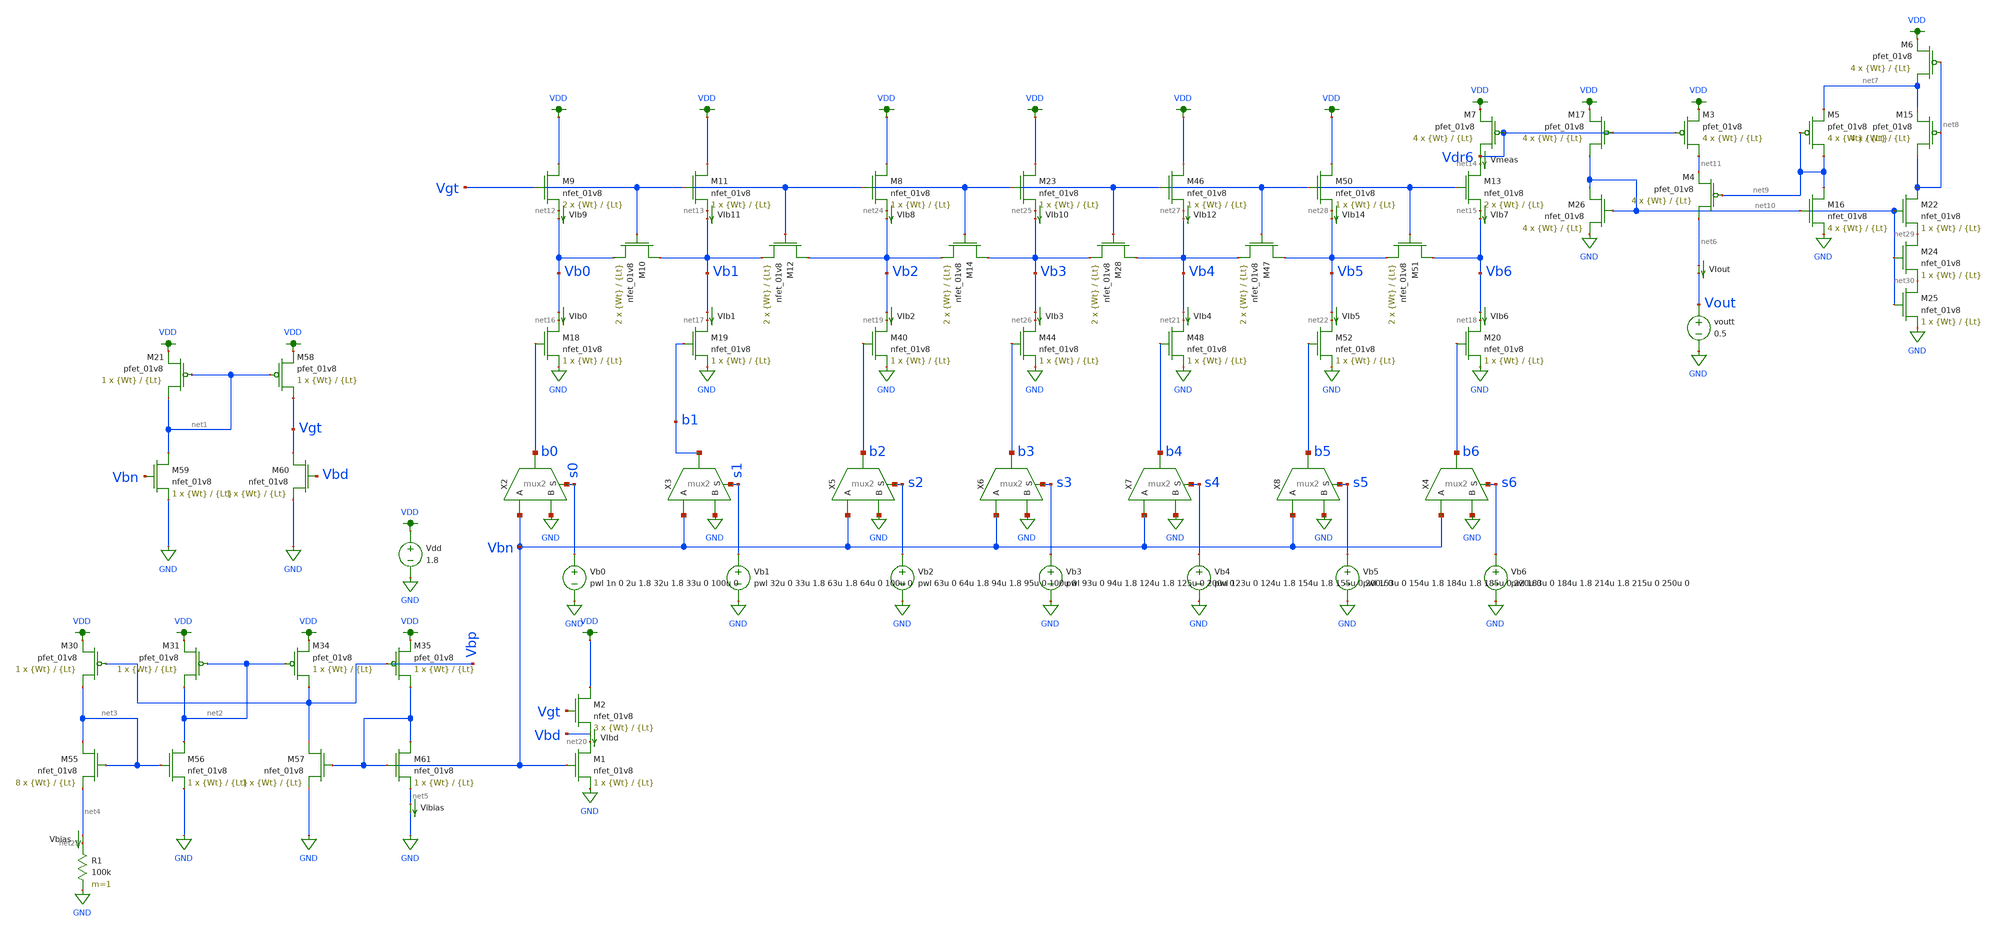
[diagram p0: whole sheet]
** sch_path: schematic/archive/dac7_test_josh_cascode_idnl.sch
**.subckt dac7_test_josh_cascode_idnl
X2 b0 Vbn GND s0 mux2
X3 b1 Vbn GND s1 mux2
Vdd VDD GND 1.8
Vb0 s0 GND pwl 1n 0 2u 1.8 32u 1.8 33u 0 100u 0
Vb1 s1 GND pwl 32u 0 33u 1.8 63u 1.8 64u 0 100u 0
Vb2 s2 GND pwl 63u 0 64u 1.8 94u 1.8 95u 0 100u 0
XM9 VDD Vgt net12 GND sky130_fd_pr__nfet_01v8 L={Lt} W={Wt} nf=1 ad='int((nf+1)/2) * W/nf * 0.29' as='int((nf+2)/2) * W/nf * 0.29'
+ pd='2*int((nf+1)/2) * (W/nf + 0.29)' ps='2*int((nf+2)/2) * (W/nf + 0.29)' nrd='0.29 / W' nrs='0.29 / W'
+ sa=0 sb=0 sd=0 mult=2 m=2
XM10 Vb1 Vgt Vb0 GND sky130_fd_pr__nfet_01v8 L={Lt} W={Wt} nf=1 ad='int((nf+1)/2) * W/nf * 0.29' as='int((nf+2)/2) * W/nf * 0.29'
+ pd='2*int((nf+1)/2) * (W/nf + 0.29)' ps='2*int((nf+2)/2) * (W/nf + 0.29)' nrd='0.29 / W' nrs='0.29 / W'
+ sa=0 sb=0 sd=0 mult=2 m=2
XM11 VDD Vgt net13 GND sky130_fd_pr__nfet_01v8 L={Lt} W={Wt} nf=1 ad='int((nf+1)/2) * W/nf * 0.29' as='int((nf+2)/2) * W/nf * 0.29'
+ pd='2*int((nf+1)/2) * (W/nf + 0.29)' ps='2*int((nf+2)/2) * (W/nf + 0.29)' nrd='0.29 / W' nrs='0.29 / W'
+ sa=0 sb=0 sd=0 mult=1 m=1
XM12 Vb2 Vgt Vb1 GND sky130_fd_pr__nfet_01v8 L={Lt} W={Wt} nf=1 ad='int((nf+1)/2) * W/nf * 0.29' as='int((nf+2)/2) * W/nf * 0.29'
+ pd='2*int((nf+1)/2) * (W/nf + 0.29)' ps='2*int((nf+2)/2) * (W/nf + 0.29)' nrd='0.29 / W' nrs='0.29 / W'
+ sa=0 sb=0 sd=0 mult=2 m=2
XM13 net14 Vgt net15 GND sky130_fd_pr__nfet_01v8 L={Lt} W={Wt} nf=1 ad='int((nf+1)/2) * W/nf * 0.29'
+ as='int((nf+2)/2) * W/nf * 0.29' pd='2*int((nf+1)/2) * (W/nf + 0.29)' ps='2*int((nf+2)/2) * (W/nf + 0.29)'
+ nrd='0.29 / W' nrs='0.29 / W' sa=0 sb=0 sd=0 mult=2 m=2
XM18 net16 b0 GND GND sky130_fd_pr__nfet_01v8 L={Lt} W={Wt} nf=1 ad='int((nf+1)/2) * W/nf * 0.29' as='int((nf+2)/2) * W/nf * 0.29'
+ pd='2*int((nf+1)/2) * (W/nf + 0.29)' ps='2*int((nf+2)/2) * (W/nf + 0.29)' nrd='0.29 / W' nrs='0.29 / W'
+ sa=0 sb=0 sd=0 mult=1 m=1
XM19 net17 b1 GND GND sky130_fd_pr__nfet_01v8 L={Lt} W={Wt} nf=1 ad='int((nf+1)/2) * W/nf * 0.29' as='int((nf+2)/2) * W/nf * 0.29'
+ pd='2*int((nf+1)/2) * (W/nf + 0.29)' ps='2*int((nf+2)/2) * (W/nf + 0.29)' nrd='0.29 / W' nrs='0.29 / W'
+ sa=0 sb=0 sd=0 mult=1 m=1
XM20 net18 b6 GND GND sky130_fd_pr__nfet_01v8 L={Lt} W={Wt} nf=1 ad='int((nf+1)/2) * W/nf * 0.29' as='int((nf+2)/2) * W/nf * 0.29'
+ pd='2*int((nf+1)/2) * (W/nf + 0.29)' ps='2*int((nf+2)/2) * (W/nf + 0.29)' nrd='0.29 / W' nrs='0.29 / W'
+ sa=0 sb=0 sd=0 mult=1 m=1
Vmeas Vdr6 net14 0
.save i(vmeas)
VIb0 Vb0 net16 0
.save i(vib0)
VIb1 Vb1 net17 0
.save i(vib1)
VIb2 Vb2 net19 0
.save i(vib2)
XM1 net20 Vbn GND GND sky130_fd_pr__nfet_01v8 L={Lt} W={Wt} nf=1 ad='int((nf+1)/2) * W/nf * 0.29' as='int((nf+2)/2) * W/nf * 0.29'
+ pd='2*int((nf+1)/2) * (W/nf + 0.29)' ps='2*int((nf+2)/2) * (W/nf + 0.29)' nrd='0.29 / W' nrs='0.29 / W'
+ sa=0 sb=0 sd=0 mult=1 m=1
VIbd Vbd net20 0
.save i(vibd)
VIb4 Vb4 net21 0
.save i(vib4)
VIb5 Vb5 net22 0
.save i(vib5)
VIb6 Vb6 net18 0
.save i(vib6)
VIout net6 Vout 0
.save i(viout)
XM2 VDD Vgt Vbd GND sky130_fd_pr__nfet_01v8 L={Lt} W={Wt} nf=1 ad='int((nf+1)/2) * W/nf * 0.29' as='int((nf+2)/2) * W/nf * 0.29'
+ pd='2*int((nf+1)/2) * (W/nf + 0.29)' ps='2*int((nf+2)/2) * (W/nf + 0.29)' nrd='0.29 / W' nrs='0.29 / W'
+ sa=0 sb=0 sd=0 mult=3 m=3
XM21 net1 net1 VDD VDD sky130_fd_pr__pfet_01v8 L={Lt} W={Wt} nf=1 ad='int((nf+1)/2) * W/nf * 0.29' as='int((nf+2)/2) * W/nf * 0.29'
+ pd='2*int((nf+1)/2) * (W/nf + 0.29)' ps='2*int((nf+2)/2) * (W/nf + 0.29)' nrd='0.29 / W' nrs='0.29 / W'
+ sa=0 sb=0 sd=0 mult=1 m=1
XM58 Vgt net1 VDD VDD sky130_fd_pr__pfet_01v8 L={Lt} W={Wt} nf=1 ad='int((nf+1)/2) * W/nf * 0.29' as='int((nf+2)/2) * W/nf * 0.29'
+ pd='2*int((nf+1)/2) * (W/nf + 0.29)' ps='2*int((nf+2)/2) * (W/nf + 0.29)' nrd='0.29 / W' nrs='0.29 / W'
+ sa=0 sb=0 sd=0 mult=1 m=1
XM59 net1 Vbn GND GND sky130_fd_pr__nfet_01v8 L={Lt} W={Wt} nf=1 ad='int((nf+1)/2) * W/nf * 0.29' as='int((nf+2)/2) * W/nf * 0.29'
+ pd='2*int((nf+1)/2) * (W/nf + 0.29)' ps='2*int((nf+2)/2) * (W/nf + 0.29)' nrd='0.29 / W' nrs='0.29 / W'
+ sa=0 sb=0 sd=0 mult=1 m=1
XM60 Vgt Vbd GND GND sky130_fd_pr__nfet_01v8 L={Lt} W={Wt} nf=1 ad='int((nf+1)/2) * W/nf * 0.29' as='int((nf+2)/2) * W/nf * 0.29'
+ pd='2*int((nf+1)/2) * (W/nf + 0.29)' ps='2*int((nf+2)/2) * (W/nf + 0.29)' nrd='0.29 / W' nrs='0.29 / W'
+ sa=0 sb=0 sd=0 mult=1 m=1
R1 net23 GND 100k m=1
Vbias net4 net23 0
.save i(vbias)
X5 b2 Vbn GND s2 mux2
Vb3 s3 GND pwl 93u 0 94u 1.8 124u 1.8 125u 0 200u 0
XM8 VDD Vgt net24 GND sky130_fd_pr__nfet_01v8 L={Lt} W={Wt} nf=1 ad='int((nf+1)/2) * W/nf * 0.29' as='int((nf+2)/2) * W/nf * 0.29'
+ pd='2*int((nf+1)/2) * (W/nf + 0.29)' ps='2*int((nf+2)/2) * (W/nf + 0.29)' nrd='0.29 / W' nrs='0.29 / W'
+ sa=0 sb=0 sd=0 mult=1 m=1
XM14 Vb3 Vgt Vb2 GND sky130_fd_pr__nfet_01v8 L={Lt} W={Wt} nf=1 ad='int((nf+1)/2) * W/nf * 0.29' as='int((nf+2)/2) * W/nf * 0.29'
+ pd='2*int((nf+1)/2) * (W/nf + 0.29)' ps='2*int((nf+2)/2) * (W/nf + 0.29)' nrd='0.29 / W' nrs='0.29 / W'
+ sa=0 sb=0 sd=0 mult=2 m=2
XM40 net19 b2 GND GND sky130_fd_pr__nfet_01v8 L={Lt} W={Wt} nf=1 ad='int((nf+1)/2) * W/nf * 0.29' as='int((nf+2)/2) * W/nf * 0.29'
+ pd='2*int((nf+1)/2) * (W/nf + 0.29)' ps='2*int((nf+2)/2) * (W/nf + 0.29)' nrd='0.29 / W' nrs='0.29 / W'
+ sa=0 sb=0 sd=0 mult=1 m=1
VIb7 net15 Vb6 0
.save i(vib7)
VIb8 net24 Vb2 0
.save i(vib8)
X6 b3 Vbn GND s3 mux2
Vb4 s4 GND pwl 123u 0 124u 1.8 154u 1.8 155u 0 200u 0
XM23 VDD Vgt net25 GND sky130_fd_pr__nfet_01v8 L={Lt} W={Wt} nf=1 ad='int((nf+1)/2) * W/nf * 0.29' as='int((nf+2)/2) * W/nf * 0.29'
+ pd='2*int((nf+1)/2) * (W/nf + 0.29)' ps='2*int((nf+2)/2) * (W/nf + 0.29)' nrd='0.29 / W' nrs='0.29 / W'
+ sa=0 sb=0 sd=0 mult=1 m=1
XM28 Vb4 Vgt Vb3 GND sky130_fd_pr__nfet_01v8 L={Lt} W={Wt} nf=1 ad='int((nf+1)/2) * W/nf * 0.29' as='int((nf+2)/2) * W/nf * 0.29'
+ pd='2*int((nf+1)/2) * (W/nf + 0.29)' ps='2*int((nf+2)/2) * (W/nf + 0.29)' nrd='0.29 / W' nrs='0.29 / W'
+ sa=0 sb=0 sd=0 mult=2 m=2
XM44 net26 b3 GND GND sky130_fd_pr__nfet_01v8 L={Lt} W={Wt} nf=1 ad='int((nf+1)/2) * W/nf * 0.29' as='int((nf+2)/2) * W/nf * 0.29'
+ pd='2*int((nf+1)/2) * (W/nf + 0.29)' ps='2*int((nf+2)/2) * (W/nf + 0.29)' nrd='0.29 / W' nrs='0.29 / W'
+ sa=0 sb=0 sd=0 mult=1 m=1
VIb3 Vb3 net26 0
.save i(vib3)
VIb10 net25 Vb3 0
.save i(vib10)
X7 b4 Vbn GND s4 mux2
Vb5 s5 GND pwl 153u 0 154u 1.8 184u 1.8 185u 0 220u 0
XM46 VDD Vgt net27 GND sky130_fd_pr__nfet_01v8 L={Lt} W={Wt} nf=1 ad='int((nf+1)/2) * W/nf * 0.29' as='int((nf+2)/2) * W/nf * 0.29'
+ pd='2*int((nf+1)/2) * (W/nf + 0.29)' ps='2*int((nf+2)/2) * (W/nf + 0.29)' nrd='0.29 / W' nrs='0.29 / W'
+ sa=0 sb=0 sd=0 mult=1 m=1
XM47 Vb5 Vgt Vb4 GND sky130_fd_pr__nfet_01v8 L={Lt} W={Wt} nf=1 ad='int((nf+1)/2) * W/nf * 0.29' as='int((nf+2)/2) * W/nf * 0.29'
+ pd='2*int((nf+1)/2) * (W/nf + 0.29)' ps='2*int((nf+2)/2) * (W/nf + 0.29)' nrd='0.29 / W' nrs='0.29 / W'
+ sa=0 sb=0 sd=0 mult=2 m=2
XM48 net21 b4 GND GND sky130_fd_pr__nfet_01v8 L={Lt} W={Wt} nf=1 ad='int((nf+1)/2) * W/nf * 0.29' as='int((nf+2)/2) * W/nf * 0.29'
+ pd='2*int((nf+1)/2) * (W/nf + 0.29)' ps='2*int((nf+2)/2) * (W/nf + 0.29)' nrd='0.29 / W' nrs='0.29 / W'
+ sa=0 sb=0 sd=0 mult=1 m=1
VIb9 net12 Vb0 0
.save i(vib9)
VIb12 net27 Vb4 0
.save i(vib12)
X8 b5 Vbn GND s5 mux2
XM50 VDD Vgt net28 GND sky130_fd_pr__nfet_01v8 L={Lt} W={Wt} nf=1 ad='int((nf+1)/2) * W/nf * 0.29' as='int((nf+2)/2) * W/nf * 0.29'
+ pd='2*int((nf+1)/2) * (W/nf + 0.29)' ps='2*int((nf+2)/2) * (W/nf + 0.29)' nrd='0.29 / W' nrs='0.29 / W'
+ sa=0 sb=0 sd=0 mult=1 m=1
XM51 Vb6 Vgt Vb5 GND sky130_fd_pr__nfet_01v8 L={Lt} W={Wt} nf=1 ad='int((nf+1)/2) * W/nf * 0.29' as='int((nf+2)/2) * W/nf * 0.29'
+ pd='2*int((nf+1)/2) * (W/nf + 0.29)' ps='2*int((nf+2)/2) * (W/nf + 0.29)' nrd='0.29 / W' nrs='0.29 / W'
+ sa=0 sb=0 sd=0 mult=2 m=2
XM52 net22 b5 GND GND sky130_fd_pr__nfet_01v8 L={Lt} W={Wt} nf=1 ad='int((nf+1)/2) * W/nf * 0.29' as='int((nf+2)/2) * W/nf * 0.29'
+ pd='2*int((nf+1)/2) * (W/nf + 0.29)' ps='2*int((nf+2)/2) * (W/nf + 0.29)' nrd='0.29 / W' nrs='0.29 / W'
+ sa=0 sb=0 sd=0 mult=1 m=1
VIb11 net13 Vb1 0
.save i(vib11)
VIb14 net28 Vb5 0
.save i(vib14)
Vb6 s6 GND pwl 183u 0 184u 1.8 214u 1.8 215u 0 250u 0
X4 b6 Vbn GND s6 mux2
XM30 net3 Vbp VDD VDD sky130_fd_pr__pfet_01v8 L={Lt} W={Wt} nf=1 ad='int((nf+1)/2) * W/nf * 0.29' as='int((nf+2)/2) * W/nf * 0.29'
+ pd='2*int((nf+1)/2) * (W/nf + 0.29)' ps='2*int((nf+2)/2) * (W/nf + 0.29)' nrd='0.29 / W' nrs='0.29 / W'
+ sa=0 sb=0 sd=0 mult=1 m=1
XM31 net2 net2 VDD VDD sky130_fd_pr__pfet_01v8 L={Lt} W={Wt} nf=1 ad='int((nf+1)/2) * W/nf * 0.29' as='int((nf+2)/2) * W/nf * 0.29'
+ pd='2*int((nf+1)/2) * (W/nf + 0.29)' ps='2*int((nf+2)/2) * (W/nf + 0.29)' nrd='0.29 / W' nrs='0.29 / W'
+ sa=0 sb=0 sd=0 mult=1 m=1
XM34 Vbp net2 VDD VDD sky130_fd_pr__pfet_01v8 L={Lt} W={Wt} nf=1 ad='int((nf+1)/2) * W/nf * 0.29' as='int((nf+2)/2) * W/nf * 0.29'
+ pd='2*int((nf+1)/2) * (W/nf + 0.29)' ps='2*int((nf+2)/2) * (W/nf + 0.29)' nrd='0.29 / W' nrs='0.29 / W'
+ sa=0 sb=0 sd=0 mult=1 m=1
XM35 Vbn Vbp VDD VDD sky130_fd_pr__pfet_01v8 L={Lt} W={Wt} nf=1 ad='int((nf+1)/2) * W/nf * 0.29' as='int((nf+2)/2) * W/nf * 0.29'
+ pd='2*int((nf+1)/2) * (W/nf + 0.29)' ps='2*int((nf+2)/2) * (W/nf + 0.29)' nrd='0.29 / W' nrs='0.29 / W'
+ sa=0 sb=0 sd=0 mult=1 m=1
XM55 net3 net3 net4 GND sky130_fd_pr__nfet_01v8 L={Lt} W={Wt} nf=1 ad='int((nf+1)/2) * W/nf * 0.29' as='int((nf+2)/2) * W/nf * 0.29'
+ pd='2*int((nf+1)/2) * (W/nf + 0.29)' ps='2*int((nf+2)/2) * (W/nf + 0.29)' nrd='0.29 / W' nrs='0.29 / W'
+ sa=0 sb=0 sd=0 mult=8 m=8
XM56 net2 net3 GND GND sky130_fd_pr__nfet_01v8 L={Lt} W={Wt} nf=1 ad='int((nf+1)/2) * W/nf * 0.29' as='int((nf+2)/2) * W/nf * 0.29'
+ pd='2*int((nf+1)/2) * (W/nf + 0.29)' ps='2*int((nf+2)/2) * (W/nf + 0.29)' nrd='0.29 / W' nrs='0.29 / W'
+ sa=0 sb=0 sd=0 mult=1 m=1
XM57 Vbp Vbn GND GND sky130_fd_pr__nfet_01v8 L={Lt} W={Wt} nf=1 ad='int((nf+1)/2) * W/nf * 0.29' as='int((nf+2)/2) * W/nf * 0.29'
+ pd='2*int((nf+1)/2) * (W/nf + 0.29)' ps='2*int((nf+2)/2) * (W/nf + 0.29)' nrd='0.29 / W' nrs='0.29 / W'
+ sa=0 sb=0 sd=0 mult=1 m=1
XM61 Vbn Vbn net5 GND sky130_fd_pr__nfet_01v8 L={Lt} W={Wt} nf=1 ad='int((nf+1)/2) * W/nf * 0.29' as='int((nf+2)/2) * W/nf * 0.29'
+ pd='2*int((nf+1)/2) * (W/nf + 0.29)' ps='2*int((nf+2)/2) * (W/nf + 0.29)' nrd='0.29 / W' nrs='0.29 / W'
+ sa=0 sb=0 sd=0 mult=1 m=1
Vibias net5 GND 0
.save i(vibias)
voutt Vout GND 0.5
XM7 Vdr6 Vdr6 VDD VDD sky130_fd_pr__pfet_01v8 L={Lt} W={Wt} nf=1 ad='int((nf+1)/2) * W/nf * 0.29' as='int((nf+2)/2) * W/nf * 0.29'
+ pd='2*int((nf+1)/2) * (W/nf + 0.29)' ps='2*int((nf+2)/2) * (W/nf + 0.29)' nrd='0.29 / W' nrs='0.29 / W'
+ sa=0 sb=0 sd=0 mult=4 m=4
XM3 net11 Vdr6 VDD VDD sky130_fd_pr__pfet_01v8 L={Lt} W={Wt} nf=1 ad='int((nf+1)/2) * W/nf * 0.29' as='int((nf+2)/2) * W/nf * 0.29'
+ pd='2*int((nf+1)/2) * (W/nf + 0.29)' ps='2*int((nf+2)/2) * (W/nf + 0.29)' nrd='0.29 / W' nrs='0.29 / W'
+ sa=0 sb=0 sd=0 mult=4 m=4
XM4 net6 net9 net11 VDD sky130_fd_pr__pfet_01v8 L={Lt} W={Wt} nf=1 ad='int((nf+1)/2) * W/nf * 0.29' as='int((nf+2)/2) * W/nf * 0.29'
+ pd='2*int((nf+1)/2) * (W/nf + 0.29)' ps='2*int((nf+2)/2) * (W/nf + 0.29)' nrd='0.29 / W' nrs='0.29 / W'
+ sa=0 sb=0 sd=0 mult=4 m=4
XM5 net9 net9 net7 VDD sky130_fd_pr__pfet_01v8 L={Lt} W={Wt} nf=1 ad='int((nf+1)/2) * W/nf * 0.29' as='int((nf+2)/2) * W/nf * 0.29'
+ pd='2*int((nf+1)/2) * (W/nf + 0.29)' ps='2*int((nf+2)/2) * (W/nf + 0.29)' nrd='0.29 / W' nrs='0.29 / W'
+ sa=0 sb=0 sd=0 mult=4 m=4
XM6 net7 net8 VDD VDD sky130_fd_pr__pfet_01v8 L={Lt} W={Wt} nf=1 ad='int((nf+1)/2) * W/nf * 0.29' as='int((nf+2)/2) * W/nf * 0.29'
+ pd='2*int((nf+1)/2) * (W/nf + 0.29)' ps='2*int((nf+2)/2) * (W/nf + 0.29)' nrd='0.29 / W' nrs='0.29 / W'
+ sa=0 sb=0 sd=0 mult=4 m=4
XM15 net8 net8 net7 VDD sky130_fd_pr__pfet_01v8 L={Lt} W={Wt} nf=1 ad='int((nf+1)/2) * W/nf * 0.29' as='int((nf+2)/2) * W/nf * 0.29'
+ pd='2*int((nf+1)/2) * (W/nf + 0.29)' ps='2*int((nf+2)/2) * (W/nf + 0.29)' nrd='0.29 / W' nrs='0.29 / W'
+ sa=0 sb=0 sd=0 mult=4 m=4
XM16 net9 net10 GND GND sky130_fd_pr__nfet_01v8 L={Lt} W={Wt} nf=1 ad='int((nf+1)/2) * W/nf * 0.29' as='int((nf+2)/2) * W/nf * 0.29'
+ pd='2*int((nf+1)/2) * (W/nf + 0.29)' ps='2*int((nf+2)/2) * (W/nf + 0.29)' nrd='0.29 / W' nrs='0.29 / W'
+ sa=0 sb=0 sd=0 mult=4 m=4
XM22 net8 net10 net29 GND sky130_fd_pr__nfet_01v8 L={Lt} W={Wt} nf=1 ad='int((nf+1)/2) * W/nf * 0.29'
+ as='int((nf+2)/2) * W/nf * 0.29' pd='2*int((nf+1)/2) * (W/nf + 0.29)' ps='2*int((nf+2)/2) * (W/nf + 0.29)'
+ nrd='0.29 / W' nrs='0.29 / W' sa=0 sb=0 sd=0 mult=1 m=1
XM24 net29 net10 net30 GND sky130_fd_pr__nfet_01v8 L={Lt} W={Wt} nf=1 ad='int((nf+1)/2) * W/nf * 0.29'
+ as='int((nf+2)/2) * W/nf * 0.29' pd='2*int((nf+1)/2) * (W/nf + 0.29)' ps='2*int((nf+2)/2) * (W/nf + 0.29)'
+ nrd='0.29 / W' nrs='0.29 / W' sa=0 sb=0 sd=0 mult=1 m=1
XM25 net30 net10 GND GND sky130_fd_pr__nfet_01v8 L={Lt} W={Wt} nf=1 ad='int((nf+1)/2) * W/nf * 0.29'
+ as='int((nf+2)/2) * W/nf * 0.29' pd='2*int((nf+1)/2) * (W/nf + 0.29)' ps='2*int((nf+2)/2) * (W/nf + 0.29)'
+ nrd='0.29 / W' nrs='0.29 / W' sa=0 sb=0 sd=0 mult=1 m=1
XM17 net10 Vdr6 VDD VDD sky130_fd_pr__pfet_01v8 L={Lt} W={Wt} nf=1 ad='int((nf+1)/2) * W/nf * 0.29' as='int((nf+2)/2) * W/nf * 0.29'
+ pd='2*int((nf+1)/2) * (W/nf + 0.29)' ps='2*int((nf+2)/2) * (W/nf + 0.29)' nrd='0.29 / W' nrs='0.29 / W'
+ sa=0 sb=0 sd=0 mult=4 m=4
XM26 net10 net10 GND GND sky130_fd_pr__nfet_01v8 L={Lt} W={Wt} nf=1 ad='int((nf+1)/2) * W/nf * 0.29'
+ as='int((nf+2)/2) * W/nf * 0.29' pd='2*int((nf+1)/2) * (W/nf + 0.29)' ps='2*int((nf+2)/2) * (W/nf + 0.29)'
+ nrd='0.29 / W' nrs='0.29 / W' sa=0 sb=0 sd=0 mult=4 m=4
**** begin user architecture code

.option wnflag=1
.param MC_SWITCH=1.0
.lib ~/skywater/skywater-pdk/libraries/sky130_fd_pr_ngspice/latest/models/sky130.lib.spice tt


.param Wt = 16
.param Lt = 4
.control
*** change W and L for the next two lines as well !***
  let myW = 16
  let myL = 4
  set wr_singlescale
  let runs = 10
  let run = 1
  while run <= runs
    set appendwrite = FALSE
    set wr_vecnames
    let code = 0
    while code < 64
      if code eq 0
        let b0 = 0
      else
        let b0 = (code % 2) * 1.8
      end
      if floor(code / 2) eq 0
        let b1 = 0
      else
        let b1 = (floor(code / 2) % 2) * 1.8
      end
      if floor(code / 4) eq 0
        let b2 = 0
      else
        let b2 = (floor(code / 4) % 2) * 1.8
      end
      if floor(code / 8) eq 0
        let b3 = 0
      else
        let b3 = floor(code / 8) % 2 * 1.8
      end
      if floor(code / 16) eq 0
        let b4 = 0
      else
        let b4 = floor(code / 16) % 2 * 1.8
      end
      if floor(code / 32) eq 0
        let b5 = 0
      else
        let b5 = floor(code / 32) % 2 * 1.8
      end
      if floor(code / 64) eq 0
        let b6 = 0
      else
        let b6 = floor(code / 64) % 2 * 1.8
      end
      alter vb0 $&b0
      alter vb1 $&b1
      alter vb2 $&b2
      alter vb3 $&b3
      alter vb4 $&b4
      alter vb5 $&b5
      alter vb6 $&b6
      save v(b0) v(b1) v(b2) v(b3) v(b4) v(b5) v(b6) i(vbias) i(viout) v(vout)
      op
      wrdata ~/Documents/MADVLSI-MP4/schematic/data/dac7cass_L{$&myL}W{$&myW}op-{$&run}.txt v(b0) v(b1)
+ v(b2) v(b3) v(b4) v(b5) v(b6) i(vbias) i(viout) v(vout)
      if code eq 0
        set appendwrite
        set wr_vecnames = FALSE
      end
      let code = code + 1
    end
    reset
    let run = run + 1
  end

  set appendwrite = FALSE
  reset
  set wr_singlescale
  set wr_vecnames
  alter vb0 1.8
  alter vb1 1.8
  alter vb2 1.8
  alter vb3 1.8
  alter vb4 1.8
  alter vb5 1.8
  alter vb6 1.8
  save v(b0) v(b1) v(b2) v(b3) v(b4) v(b5) v(b6) i(vbias) i(viout) v(vout)
  dc Voutt 0 1.8 0.01
  run
  wrdata ~/Documents/MADVLSI-MP4/schematic/data/dac7cass_L{$&myL}W{$&myW}vout-1.txt v(b0) v(b1) v(b2)
+ v(b3) v(b4) v(b5) v(b6) i(vbias) i(viout) v(vout)

  reset
  set wr_singlescale
  set wr_vecnames
  alter vb0 1.8
  alter vb1 1.8
  alter vb2 1.8
  alter vb3 1.8
  alter vb4 1.8
  alter vb5 1.8
  alter vb6 0
  save v(b0) v(b1) v(b2) v(b3) v(b4) v(b5) v(b6) i(vbias) i(viout) v(vout)
  dc Voutt 0 1.8 0.01
  run
  wrdata ~/Documents/MADVLSI-MP4/schematic/data/dac7cass_L{$&myL}W{$&myW}vout-2.txt v(b0) v(b1) v(b2)
+ v(b3) v(b4) v(b5) v(b6) i(vbias) i(viout) v(vout)

  reset
  set wr_singlescale
  set wr_vecnames
  alter vb0 1.8
  alter vb1 1.8
  alter vb2 1.8
  alter vb3 1.8
  alter vb4 1.8
  alter vb5 1.8
  alter vb6 1.8
  save v(b0) v(b1) v(b2) v(b3) v(b4) v(b5) v(b6) i(vbias) i(viout) v(vout)
  dc Vdd 0 1.8 0.01
  run
  wrdata ~/Documents/MADVLSI-MP4/schematic/data/dac7cass_L{$&myL}W{$&myW}vdd-1.txt v(b0) v(b1) v(b2)
+ v(b3) v(b4) v(b5) v(b6) i(vbias) i(viout) v(vout)

  reset
  set wr_singlescale
  set wr_vecnames
  alter vb0 1.8
  alter vb1 1.8
  alter vb2 1.8
  alter vb3 1.8
  alter vb4 1.8
  alter vb5 1.8
  alter vb6 0
  save v(b0) v(b1) v(b2) v(b3) v(b4) v(b5) v(b6) i(vbias) i(viout) v(vout)
  dc Vdd 0 1.8 0.01
  run
  wrdata ~/Documents/MADVLSI-MP4/schematic/data/dac7cass_L{$&myL}W{$&myW}vdd-2.txt v(b0) v(b1) v(b2)
+ v(b3) v(b4) v(b5) v(b6) i(vbias) i(viout) v(vout)
.endc

**** end user architecture code
**.ends
.GLOBAL GND
.GLOBAL VDD
.end
